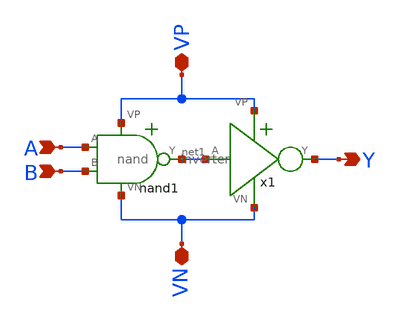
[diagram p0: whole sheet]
** sch_path: mp1/and/and.sch
**.subckt and A B VP VN Y
*.ipin A
*.ipin B
*.iopin VP
*.iopin VN
*.opin Y
nand1 VP net1 A B VN nand
x1 VP net1 Y VN inverter
**.ends

* expanding   symbol:  /home/madvlsi/Documents/vlsi/mp1/and/nand.sym # of pins=5
** sym_path: mp1/and/nand.sym
** sch_path: mp1/and/nand.sch
.subckt nand VP Y A B VN
*.ipin A
*.ipin B
*.iopin VP
*.iopin VN
*.opin Y
XM1 net1 B VN VN sky130_fd_pr__nfet_01v8 L=0.15 W=1 nf=1 ad='int((nf+1)/2) * W/nf * 0.29' as='int((nf+2)/2) * W/nf * 0.29'
+ pd='2*int((nf+1)/2) * (W/nf + 0.29)' ps='2*int((nf+2)/2) * (W/nf + 0.29)' nrd='0.29 / W' nrs='0.29 / W'
+ sa=0 sb=0 sd=0 mult=1 m=1
XM2 Y A net1 net1 sky130_fd_pr__nfet_01v8 L=0.15 W=1 nf=1 ad='int((nf+1)/2) * W/nf * 0.29' as='int((nf+2)/2) * W/nf * 0.29'
+ pd='2*int((nf+1)/2) * (W/nf + 0.29)' ps='2*int((nf+2)/2) * (W/nf + 0.29)' nrd='0.29 / W' nrs='0.29 / W'
+ sa=0 sb=0 sd=0 mult=1 m=1
XM3 Y A VP VP sky130_fd_pr__pfet_01v8 L=0.15 W=1 nf=1 ad='int((nf+1)/2) * W/nf * 0.29' as='int((nf+2)/2) * W/nf * 0.29'
+ pd='2*int((nf+1)/2) * (W/nf + 0.29)' ps='2*int((nf+2)/2) * (W/nf + 0.29)' nrd='0.29 / W' nrs='0.29 / W'
+ sa=0 sb=0 sd=0 mult=1 m=1
XM4 Y B VP VP sky130_fd_pr__pfet_01v8 L=0.15 W=1 nf=1 ad='int((nf+1)/2) * W/nf * 0.29' as='int((nf+2)/2) * W/nf * 0.29'
+ pd='2*int((nf+1)/2) * (W/nf + 0.29)' ps='2*int((nf+2)/2) * (W/nf + 0.29)' nrd='0.29 / W' nrs='0.29 / W'
+ sa=0 sb=0 sd=0 mult=1 m=1
.ends


* expanding   symbol:  /home/madvlsi/Documents/vlsi/mp1/inverter/inverter.sym # of pins=4
** sym_path: mp1/inverter/inverter.sym
** sch_path: mp1/inverter/inverter.sch
.subckt inverter VP A Y VN
*.iopin VP
*.iopin VN
*.ipin A
*.opin Y
XM1 Y A VN VN sky130_fd_pr__nfet_01v8 L=0.15 W=1 nf=1 ad='int((nf+1)/2) * W/nf * 0.29' as='int((nf+2)/2) * W/nf * 0.29'
+ pd='2*int((nf+1)/2) * (W/nf + 0.29)' ps='2*int((nf+2)/2) * (W/nf + 0.29)' nrd='0.29 / W' nrs='0.29 / W'
+ sa=0 sb=0 sd=0 mult=1 m=1
XM2 Y A VP VP sky130_fd_pr__pfet_01v8 L=0.15 W=1 nf=1 ad='int((nf+1)/2) * W/nf * 0.29' as='int((nf+2)/2) * W/nf * 0.29'
+ pd='2*int((nf+1)/2) * (W/nf + 0.29)' ps='2*int((nf+2)/2) * (W/nf + 0.29)' nrd='0.29 / W' nrs='0.29 / W'
+ sa=0 sb=0 sd=0 mult=1 m=1
.ends

.end
